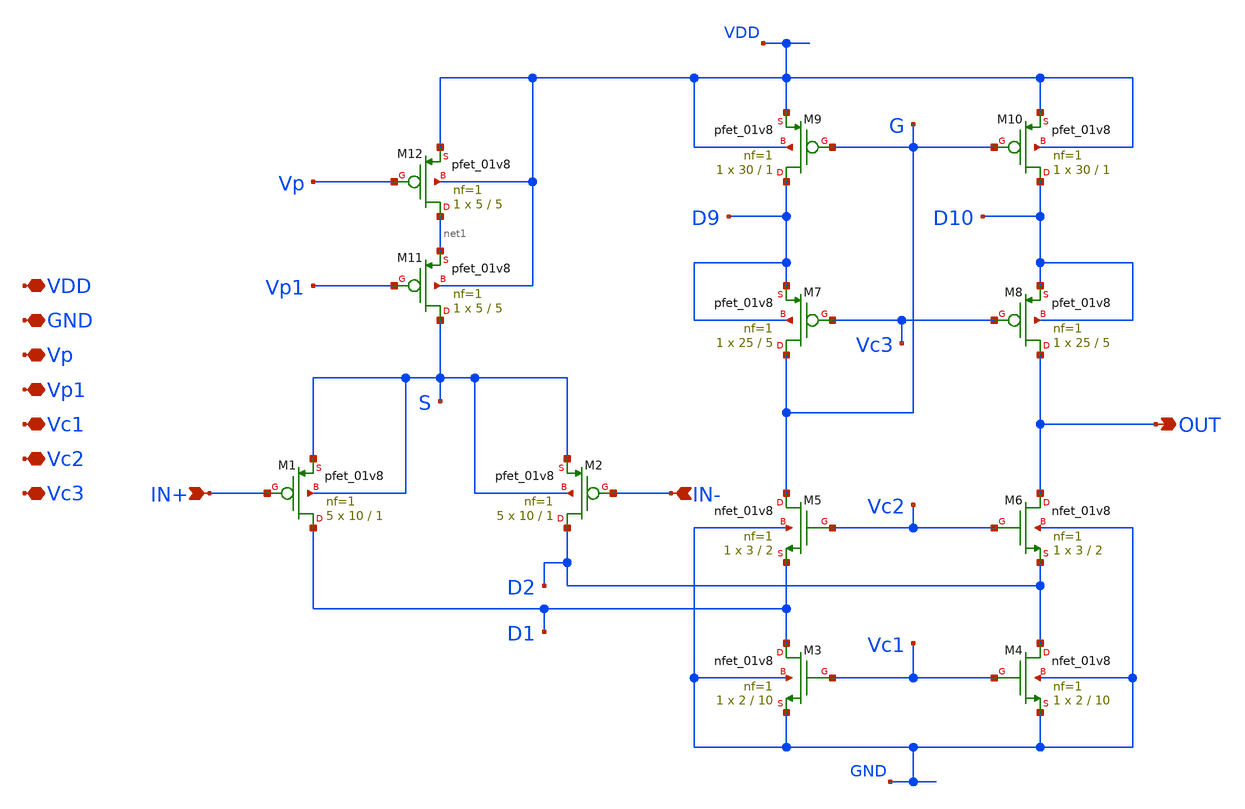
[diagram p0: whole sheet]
** sch_path: xschem/untitled.sch
**.subckt untitled IN+ IN- OUT VDD GND Vp Vp1 Vc1 Vc2 Vc3
*.ipin IN+
*.ipin IN-
*.opin OUT
*.iopin VDD
*.iopin GND
*.iopin Vp
*.iopin Vp1
*.iopin Vc1
*.iopin Vc2
*.iopin Vc3
XM1 D1 IN+ S S sky130_fd_pr__pfet_01v8 L=1 W=10 nf=1 ad='int((nf+1)/2) * W/nf * 0.29' as='int((nf+2)/2) * W/nf * 0.29'
+ pd='2*int((nf+1)/2) * (W/nf + 0.29)' ps='2*int((nf+2)/2) * (W/nf + 0.29)' nrd='0.29 / W' nrs='0.29 / W'
+ sa=0 sb=0 sd=0 mult=5 m=5
XM2 D2 IN- S S sky130_fd_pr__pfet_01v8 L=1 W=10 nf=1 ad='int((nf+1)/2) * W/nf * 0.29' as='int((nf+2)/2) * W/nf * 0.29'
+ pd='2*int((nf+1)/2) * (W/nf + 0.29)' ps='2*int((nf+2)/2) * (W/nf + 0.29)' nrd='0.29 / W' nrs='0.29 / W'
+ sa=0 sb=0 sd=0 mult=5 m=5
XM3 D1 Vc1 GND GND sky130_fd_pr__nfet_01v8 L=10 W=2 nf=1 ad='int((nf+1)/2) * W/nf * 0.29' as='int((nf+2)/2) * W/nf * 0.29'
+ pd='2*int((nf+1)/2) * (W/nf + 0.29)' ps='2*int((nf+2)/2) * (W/nf + 0.29)' nrd='0.29 / W' nrs='0.29 / W'
+ sa=0 sb=0 sd=0 mult=1 m=1
XM4 D2 Vc1 GND GND sky130_fd_pr__nfet_01v8 L=10 W=2 nf=1 ad='int((nf+1)/2) * W/nf * 0.29' as='int((nf+2)/2) * W/nf * 0.29'
+ pd='2*int((nf+1)/2) * (W/nf + 0.29)' ps='2*int((nf+2)/2) * (W/nf + 0.29)' nrd='0.29 / W' nrs='0.29 / W'
+ sa=0 sb=0 sd=0 mult=1 m=1
XM5 G Vc2 D1 GND sky130_fd_pr__nfet_01v8 L=2 W=3 nf=1 ad='int((nf+1)/2) * W/nf * 0.29' as='int((nf+2)/2) * W/nf * 0.29'
+ pd='2*int((nf+1)/2) * (W/nf + 0.29)' ps='2*int((nf+2)/2) * (W/nf + 0.29)' nrd='0.29 / W' nrs='0.29 / W'
+ sa=0 sb=0 sd=0 mult=1 m=1
XM6 OUT Vc2 D2 GND sky130_fd_pr__nfet_01v8 L=2 W=3 nf=1 ad='int((nf+1)/2) * W/nf * 0.29' as='int((nf+2)/2) * W/nf * 0.29'
+ pd='2*int((nf+1)/2) * (W/nf + 0.29)' ps='2*int((nf+2)/2) * (W/nf + 0.29)' nrd='0.29 / W' nrs='0.29 / W'
+ sa=0 sb=0 sd=0 mult=1 m=1
XM7 G Vc3 D9 D9 sky130_fd_pr__pfet_01v8 L=5 W=25 nf=1 ad='int((nf+1)/2) * W/nf * 0.29' as='int((nf+2)/2) * W/nf * 0.29'
+ pd='2*int((nf+1)/2) * (W/nf + 0.29)' ps='2*int((nf+2)/2) * (W/nf + 0.29)' nrd='0.29 / W' nrs='0.29 / W'
+ sa=0 sb=0 sd=0 mult=1 m=1
XM8 OUT Vc3 D10 D10 sky130_fd_pr__pfet_01v8 L=5 W=25 nf=1 ad='int((nf+1)/2) * W/nf * 0.29' as='int((nf+2)/2) * W/nf * 0.29'
+ pd='2*int((nf+1)/2) * (W/nf + 0.29)' ps='2*int((nf+2)/2) * (W/nf + 0.29)' nrd='0.29 / W' nrs='0.29 / W'
+ sa=0 sb=0 sd=0 mult=1 m=1
XM9 D9 G VDD VDD sky130_fd_pr__pfet_01v8 L=1 W=30 nf=1 ad='int((nf+1)/2) * W/nf * 0.29' as='int((nf+2)/2) * W/nf * 0.29'
+ pd='2*int((nf+1)/2) * (W/nf + 0.29)' ps='2*int((nf+2)/2) * (W/nf + 0.29)' nrd='0.29 / W' nrs='0.29 / W'
+ sa=0 sb=0 sd=0 mult=1 m=1
XM10 D10 G VDD VDD sky130_fd_pr__pfet_01v8 L=1 W=30 nf=1 ad='int((nf+1)/2) * W/nf * 0.29' as='int((nf+2)/2) * W/nf * 0.29'
+ pd='2*int((nf+1)/2) * (W/nf + 0.29)' ps='2*int((nf+2)/2) * (W/nf + 0.29)' nrd='0.29 / W' nrs='0.29 / W'
+ sa=0 sb=0 sd=0 mult=1 m=1
XM11 S Vp1 net1 VDD sky130_fd_pr__pfet_01v8 L=5 W=5 nf=1 ad='int((nf+1)/2) * W/nf * 0.29' as='int((nf+2)/2) * W/nf * 0.29'
+ pd='2*int((nf+1)/2) * (W/nf + 0.29)' ps='2*int((nf+2)/2) * (W/nf + 0.29)' nrd='0.29 / W' nrs='0.29 / W'
+ sa=0 sb=0 sd=0 mult=1 m=1
XM12 net1 Vp VDD VDD sky130_fd_pr__pfet_01v8 L=5 W=5 nf=1 ad='int((nf+1)/2) * W/nf * 0.29' as='int((nf+2)/2) * W/nf * 0.29'
+ pd='2*int((nf+1)/2) * (W/nf + 0.29)' ps='2*int((nf+2)/2) * (W/nf + 0.29)' nrd='0.29 / W' nrs='0.29 / W'
+ sa=0 sb=0 sd=0 mult=1 m=1
**.ends
.end
